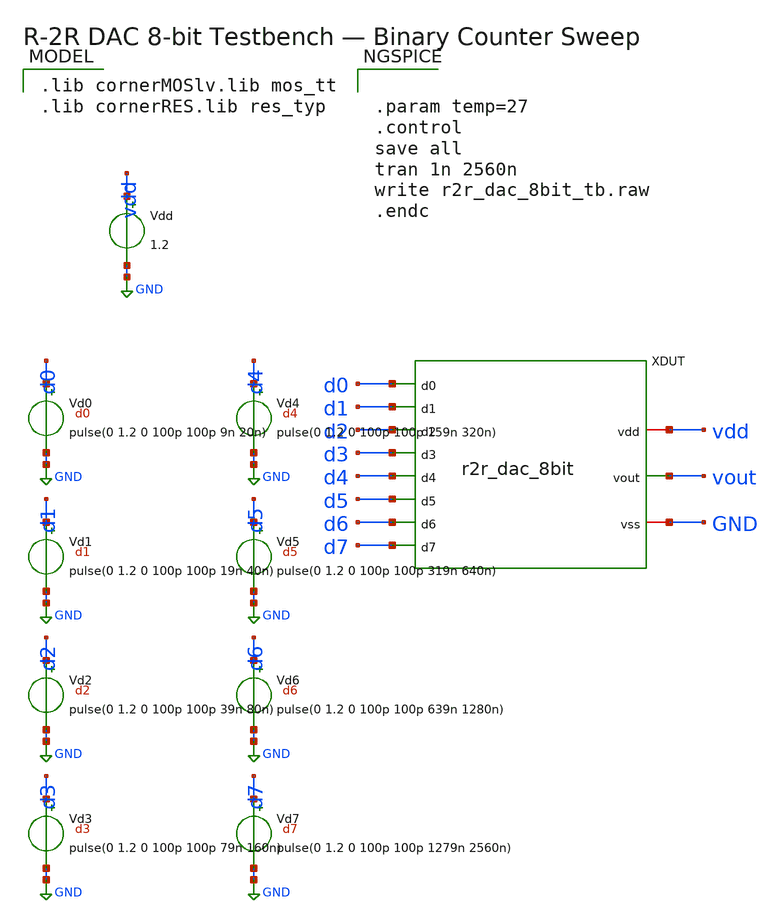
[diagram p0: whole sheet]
** sch_path: xschem/r2r_dac_8bit_tb.sch
**.subckt r2r_dac_8bit_tb
XDUT d0 d1 d2 d3 d4 d5 d6 d7 vdd vout GND r2r_dac_8bit
Vdd vdd GND 1.2
Vd0 d0 GND pulse(0 1.2 0 100p 100p 9n 20n)
Vd1 d1 GND pulse(0 1.2 0 100p 100p 19n 40n)
Vd2 d2 GND pulse(0 1.2 0 100p 100p 39n 80n)
Vd3 d3 GND pulse(0 1.2 0 100p 100p 79n 160n)
Vd4 d4 GND pulse(0 1.2 0 100p 100p 159n 320n)
Vd5 d5 GND pulse(0 1.2 0 100p 100p 319n 640n)
Vd6 d6 GND pulse(0 1.2 0 100p 100p 639n 1280n)
Vd7 d7 GND pulse(0 1.2 0 100p 100p 1279n 2560n)
**** begin user architecture code
 .lib cornerMOSlv.lib mos_tt
.lib cornerRES.lib res_typ



.param temp=27
.control
save all
tran 1n 2560n
write r2r_dac_8bit_tb.raw
.endc


**** end user architecture code
**.ends
.GLOBAL GND
.end
